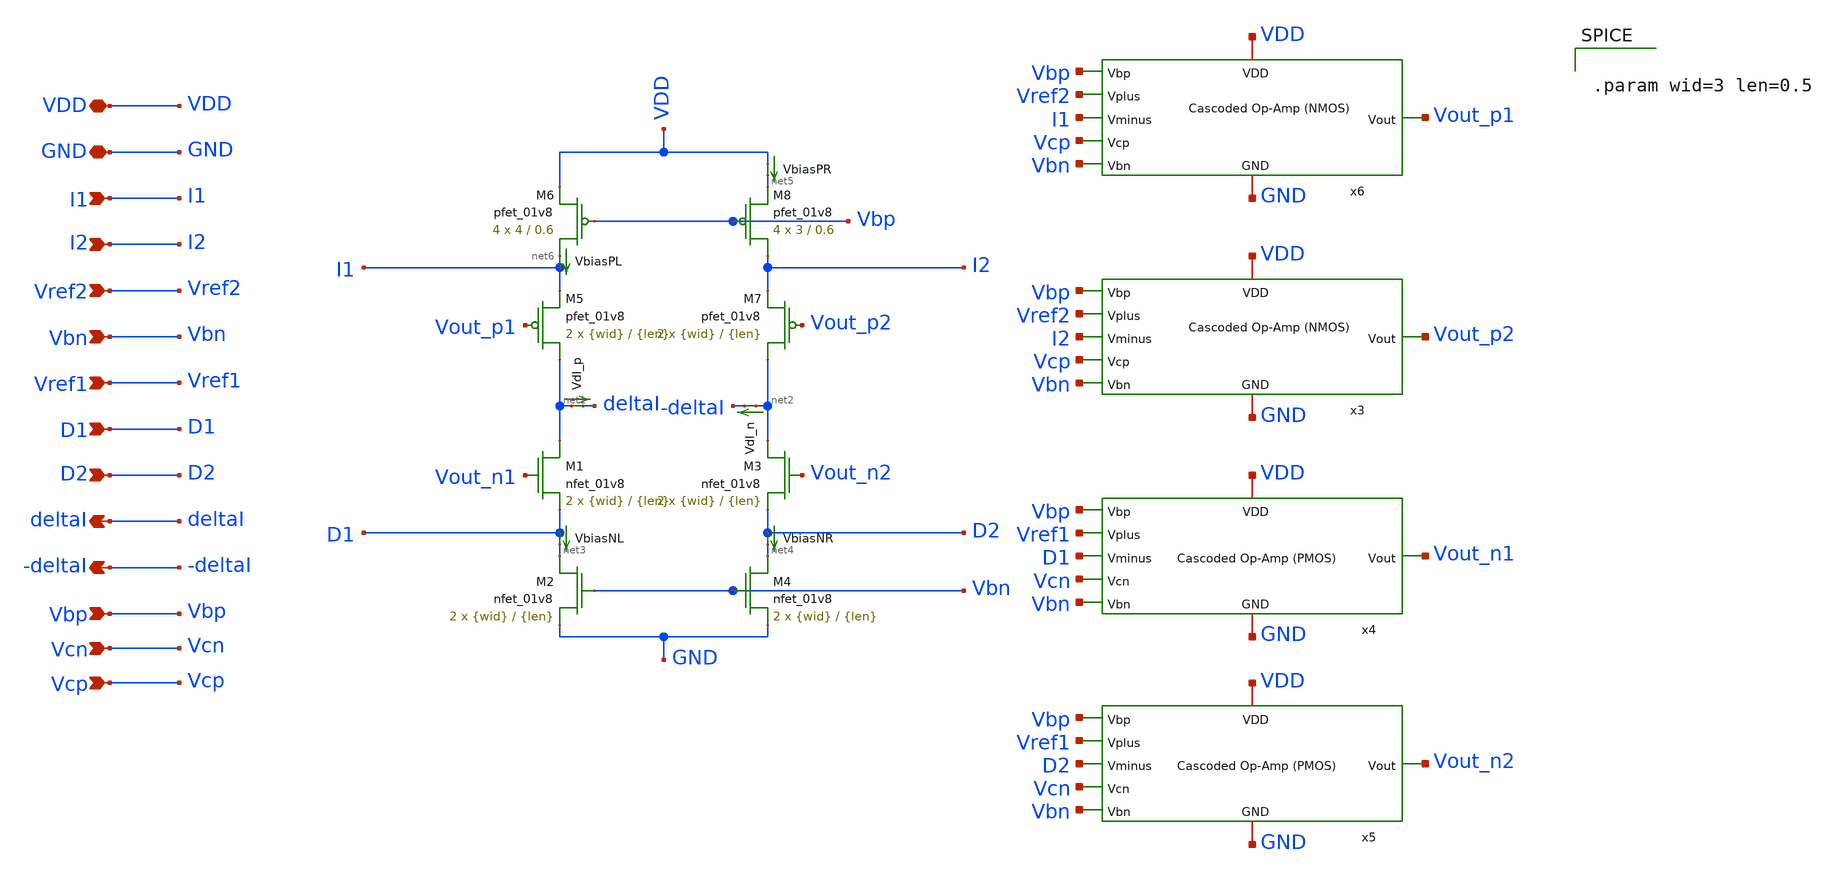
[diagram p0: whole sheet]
** sch_path: final/schematics/summation_backup.sch
**.subckt summation_backup VDD GND I1 I2 Vref2 Vbn Vref1 D1 D2 deltaI -deltaI Vbp Vcn Vcp
*.iopin VDD
*.iopin GND
*.ipin I1
*.ipin I2
*.ipin Vref2
*.ipin Vbn
*.ipin Vref1
*.ipin D1
*.ipin D2
*.opin deltaI
*.opin -deltaI
*.ipin Vbp
*.ipin Vcn
*.ipin Vcp
XM1 net1 Vout_n1 D1 GND sky130_fd_pr__nfet_01v8 L={len} W={wid} nf=1 ad='int((nf+1)/2) * W/nf * 0.29'
+ as='int((nf+2)/2) * W/nf * 0.29' pd='2*int((nf+1)/2) * (W/nf + 0.29)' ps='2*int((nf+2)/2) * (W/nf + 0.29)'
+ nrd='0.29 / W' nrs='0.29 / W' sa=0 sb=0 sd=0 mult=2 m=2
XM2 net3 Vbn GND GND sky130_fd_pr__nfet_01v8 L={len} W={wid} nf=1 ad='int((nf+1)/2) * W/nf * 0.29' as='int((nf+2)/2) * W/nf * 0.29'
+ pd='2*int((nf+1)/2) * (W/nf + 0.29)' ps='2*int((nf+2)/2) * (W/nf + 0.29)' nrd='0.29 / W' nrs='0.29 / W'
+ sa=0 sb=0 sd=0 mult=2 m=2
XM3 net2 Vout_n2 D2 GND sky130_fd_pr__nfet_01v8 L={len} W={wid} nf=1 ad='int((nf+1)/2) * W/nf * 0.29'
+ as='int((nf+2)/2) * W/nf * 0.29' pd='2*int((nf+1)/2) * (W/nf + 0.29)' ps='2*int((nf+2)/2) * (W/nf + 0.29)'
+ nrd='0.29 / W' nrs='0.29 / W' sa=0 sb=0 sd=0 mult=2 m=2
XM5 net1 Vout_p1 I1 VDD sky130_fd_pr__pfet_01v8 L={len} W={wid} nf=1 ad='int((nf+1)/2) * W/nf * 0.29'
+ as='int((nf+2)/2) * W/nf * 0.29' pd='2*int((nf+1)/2) * (W/nf + 0.29)' ps='2*int((nf+2)/2) * (W/nf + 0.29)'
+ nrd='0.29 / W' nrs='0.29 / W' sa=0 sb=0 sd=0 mult=2 m=2
XM6 net6 Vbp VDD VDD sky130_fd_pr__pfet_01v8 L=0.6 W=4 nf=1 ad='int((nf+1)/2) * W/nf * 0.29' as='int((nf+2)/2) * W/nf * 0.29'
+ pd='2*int((nf+1)/2) * (W/nf + 0.29)' ps='2*int((nf+2)/2) * (W/nf + 0.29)' nrd='0.29 / W' nrs='0.29 / W'
+ sa=0 sb=0 sd=0 mult=4 m=4
XM7 net2 Vout_p2 I2 VDD sky130_fd_pr__pfet_01v8 L={len} W={wid} nf=1 ad='int((nf+1)/2) * W/nf * 0.29'
+ as='int((nf+2)/2) * W/nf * 0.29' pd='2*int((nf+1)/2) * (W/nf + 0.29)' ps='2*int((nf+2)/2) * (W/nf + 0.29)'
+ nrd='0.29 / W' nrs='0.29 / W' sa=0 sb=0 sd=0 mult=2 m=2
XM8 I2 Vbp net5 VDD sky130_fd_pr__pfet_01v8 L=0.6 W=3 nf=1 ad='int((nf+1)/2) * W/nf * 0.29' as='int((nf+2)/2) * W/nf * 0.29'
+ pd='2*int((nf+1)/2) * (W/nf + 0.29)' ps='2*int((nf+2)/2) * (W/nf + 0.29)' nrd='0.29 / W' nrs='0.29 / W'
+ sa=0 sb=0 sd=0 mult=4 m=4
x5 Vbp Vref1 D2 Vcn Vbn VDD GND Vout_n2 cascoded_opamp_pmos
x3 Vbp Vref2 I2 Vcp Vbn VDD GND Vout_p2 cascoded_opamp
x4 Vbp Vref1 D1 Vcn Vbn VDD GND Vout_n1 cascoded_opamp_pmos
x6 Vbp Vref2 I1 Vcp Vbn VDD GND Vout_p1 cascoded_opamp
VbiasNL D1 net3 0
.save i(vbiasnl)
VbiasNR D2 net4 0
.save i(vbiasnr)
VbiasPR VDD net5 0
.save i(vbiaspr)
VbiasPL net6 I1 0
.save i(vbiaspl)
VdI_n net2 -deltaI 0
.save i(vdi_n)
VdI_p net1 deltaI 0
.save i(vdi_p)
XM4 net4 Vbn GND GND sky130_fd_pr__nfet_01v8 L={len} W={wid} nf=1 ad='int((nf+1)/2) * W/nf * 0.29' as='int((nf+2)/2) * W/nf * 0.29'
+ pd='2*int((nf+1)/2) * (W/nf + 0.29)' ps='2*int((nf+2)/2) * (W/nf + 0.29)' nrd='0.29 / W' nrs='0.29 / W'
+ sa=0 sb=0 sd=0 mult=2 m=2
**** begin user architecture code


.param wid=3 len=0.5


**** end user architecture code
**.ends
.end
